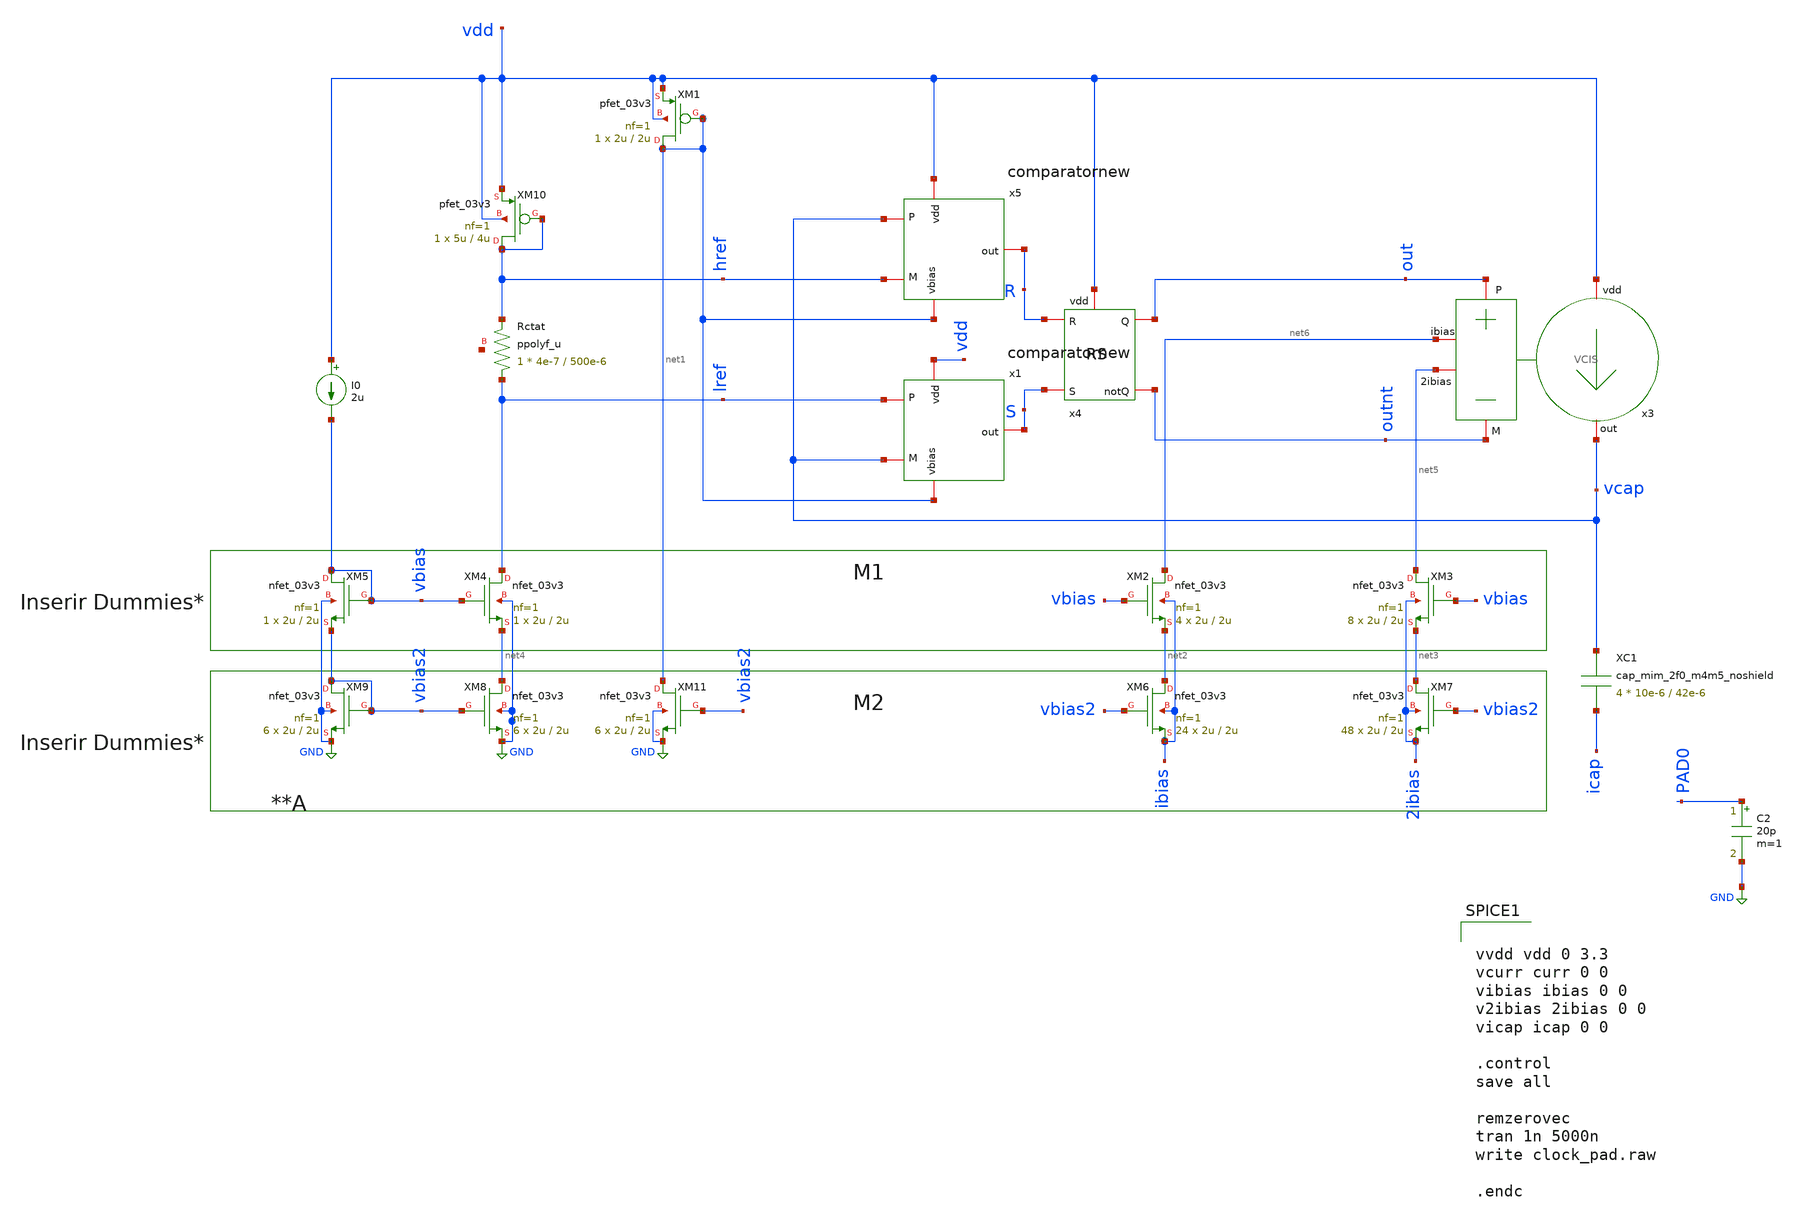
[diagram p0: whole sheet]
** sch_path: Clock_Reference/clock_pad.sch
**.subckt clock_pad
XM1 net1 net1 vdd vdd pfet_03v3 L=2u W=2u nf=1 ad='int((nf+1)/2) * W/nf * 0.18u' as='int((nf+2)/2) * W/nf * 0.18u'
+ pd='2*int((nf+1)/2) * (W/nf + 0.18u)' ps='2*int((nf+2)/2) * (W/nf + 0.18u)' nrd='0.18u / W' nrs='0.18u / W'
+ sa=0 sb=0 sd=0 m=1
XM2 net6 vbias net2 ibias nfet_03v3 L=2u W=2u nf=1 ad='int((nf+1)/2) * W/nf * 0.18u' as='int((nf+2)/2) * W/nf * 0.18u'
+ pd='2*int((nf+1)/2) * (W/nf + 0.18u)' ps='2*int((nf+2)/2) * (W/nf + 0.18u)' nrd='0.18u / W' nrs='0.18u / W'
+ sa=0 sb=0 sd=0 m=4
XM3 net5 vbias net3 2ibias nfet_03v3 L=2u W=2u nf=1 ad='int((nf+1)/2) * W/nf * 0.18u' as='int((nf+2)/2) * W/nf * 0.18u'
+ pd='2*int((nf+1)/2) * (W/nf + 0.18u)' ps='2*int((nf+2)/2) * (W/nf + 0.18u)' nrd='0.18u / W' nrs='0.18u / W'
+ sa=0 sb=0 sd=0 m=8
XM4 lref vbias net4 GND nfet_03v3 L=2u W=2u nf=1 ad='int((nf+1)/2) * W/nf * 0.18u' as='int((nf+2)/2) * W/nf * 0.18u'
+ pd='2*int((nf+1)/2) * (W/nf + 0.18u)' ps='2*int((nf+2)/2) * (W/nf + 0.18u)' nrd='0.18u / W' nrs='0.18u / W'
+ sa=0 sb=0 sd=0 m=1
XM5 vbias vbias vbias2 GND nfet_03v3 L=2u W=2u nf=1 ad='int((nf+1)/2) * W/nf * 0.18u' as='int((nf+2)/2) * W/nf * 0.18u'
+ pd='2*int((nf+1)/2) * (W/nf + 0.18u)' ps='2*int((nf+2)/2) * (W/nf + 0.18u)' nrd='0.18u / W' nrs='0.18u / W'
+ sa=0 sb=0 sd=0 m=1
I0 vdd vbias 2u
XM6 net2 vbias2 ibias ibias nfet_03v3 L=2u W=2u nf=1 ad='int((nf+1)/2) * W/nf * 0.18u' as='int((nf+2)/2) * W/nf * 0.18u'
+ pd='2*int((nf+1)/2) * (W/nf + 0.18u)' ps='2*int((nf+2)/2) * (W/nf + 0.18u)' nrd='0.18u / W' nrs='0.18u / W'
+ sa=0 sb=0 sd=0 m=24
XM7 net3 vbias2 2ibias 2ibias nfet_03v3 L=2u W=2u nf=1 ad='int((nf+1)/2) * W/nf * 0.18u' as='int((nf+2)/2) * W/nf * 0.18u'
+ pd='2*int((nf+1)/2) * (W/nf + 0.18u)' ps='2*int((nf+2)/2) * (W/nf + 0.18u)' nrd='0.18u / W' nrs='0.18u / W'
+ sa=0 sb=0 sd=0 m=48
XM8 net4 vbias2 GND GND nfet_03v3 L=2u W=2u nf=1 ad='int((nf+1)/2) * W/nf * 0.18u' as='int((nf+2)/2) * W/nf * 0.18u'
+ pd='2*int((nf+1)/2) * (W/nf + 0.18u)' ps='2*int((nf+2)/2) * (W/nf + 0.18u)' nrd='0.18u / W' nrs='0.18u / W'
+ sa=0 sb=0 sd=0 m=6
XM9 vbias2 vbias2 GND GND nfet_03v3 L=2u W=2u nf=1 ad='int((nf+1)/2) * W/nf * 0.18u' as='int((nf+2)/2) * W/nf * 0.18u'
+ pd='2*int((nf+1)/2) * (W/nf + 0.18u)' ps='2*int((nf+2)/2) * (W/nf + 0.18u)' nrd='0.18u / W' nrs='0.18u / W'
+ sa=0 sb=0 sd=0 m=6
XRctat lref href net7 ppolyf_u r_width=4e-7 r_length=500e-6 m=1
XM10 href href vdd vdd pfet_03v3 L=4u W=5u nf=1 ad='int((nf+1)/2) * W/nf * 0.18u' as='int((nf+2)/2) * W/nf * 0.18u'
+ pd='2*int((nf+1)/2) * (W/nf + 0.18u)' ps='2*int((nf+2)/2) * (W/nf + 0.18u)' nrd='0.18u / W' nrs='0.18u / W'
+ sa=0 sb=0 sd=0 m=1
XM11 net1 vbias2 GND GND nfet_03v3 L=2u W=2u nf=1 ad='int((nf+1)/2) * W/nf * 0.18u' as='int((nf+2)/2) * W/nf * 0.18u'
+ pd='2*int((nf+1)/2) * (W/nf + 0.18u)' ps='2*int((nf+2)/2) * (W/nf + 0.18u)' nrd='0.18u / W' nrs='0.18u / W'
+ sa=0 sb=0 sd=0 m=6
x3 vdd vcap out outnt net6 net5 VCIS
x4 vdd R S out outnt RS
x5 vdd net1 vcap href R comparatornew
x1 vdd net1 lref vcap S comparatornew
XC1 vcap icap cap_mim_2f0_m4m5_noshield c_width=10e-6 c_length=42e-6 m=4
C2 PAD0 GND 20p m=1
**** begin user architecture code

.include /home/gmaranhao/Desktop/Bracolin/padframe/openfasoc-io-tb/gf180mcu_fd_io.spice
.include /home/gmaranhao/Desktop/Bracolin/padframe/openfasoc-io-tb/gf180mcu_fd_io__bi_t_extracted.spice

Xc1 vdd 0 vdd 0 gf180mcu_fd_io__cor
Xf1 vdd 0 vdd 0 gf180mcu_fd_io__fill5
Xf2 vdd 0 vdd 0 gf180mcu_fd_io__fill10


Xsup1 vdd 0 0 gf180mcu_fd_io__dvdd
Xsup2 vdd 0 vdd gf180mcu_fd_io__dvss


*XDUT0 out 0 vdd 0 0 vdd PAD0 vdd 0 0 vdd 0 vdd 0 0 gf180mcu_fd_io__bi_t
XDUT1 out 0 vdd 0 0 vdd PAD0 vdd 0 0 vdd 0 vdd 0 0 gf180mcu_fd_io__bi_t_extracted



vvdd vdd 0 3.3
vcurr curr 0 0
vibias ibias 0 0
v2ibias 2ibias 0 0
vicap icap 0 0

.control
save all

remzerovec
tran 1n 5000n
write clock_pad.raw

.endc



.include $::180MCU_MODELS/design.ngspice
.lib $::180MCU_MODELS/sm141064.ngspice typical
.lib $::180MCU_MODELS/sm141064.ngspice res_typical
.lib $::180MCU_MODELS/sm141064.ngspice moscap_typical
.lib $::180MCU_MODELS/sm141064.ngspice mimcap_typical
.lib $::180MCU_MODELS/sm141064.ngspice cap_mim
.lib $::180MCU_MODELS/sm141064.ngspice diode_typical
*.lib $::180MCU_MODELS/sm141064.ngspice res_statistical
*.param sw_stat_mismatch=1
*.param sw_stat_global=1

**** end user architecture code
**.ends
.GLOBAL GND
.end
